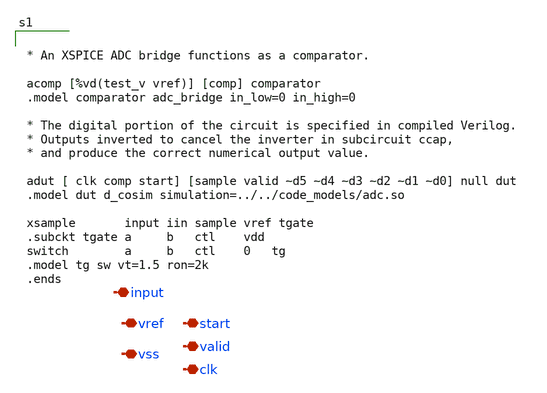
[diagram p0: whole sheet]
** sch_path: samples/digital_cosimulation/sigma_delta_counter/symbol/sigma_delta_counter.sch
**.subckt sigma_delta_counter vss vref start valid clk input
*.iopin vss
*.iopin vref
*.iopin start
*.iopin valid
*.iopin clk
*.iopin input
**** begin user architecture code


* An XSPICE ADC bridge functions as a comparator.

acomp [%vd(test_v vref)] [comp] comparator
.model comparator adc_bridge in_low=0 in_high=0

* The digital portion of the circuit is specified in compiled Verilog.
* Outputs inverted to cancel the inverter in subcircuit ccap,
* and produce the correct numerical output value.

adut [ clk comp start] [sample valid ~d5 ~d4 ~d3 ~d2 ~d1 ~d0] null dut
.model dut d_cosim simulation=../../code_models/adc.so

xsample       input iin sample vref tgate
.subckt tgate a     b   ctl    vdd
switch        a     b   ctl    0   tg
.model tg sw vt=1.5 ron=2k
.ends


**** end user architecture code
**.ends
.end
